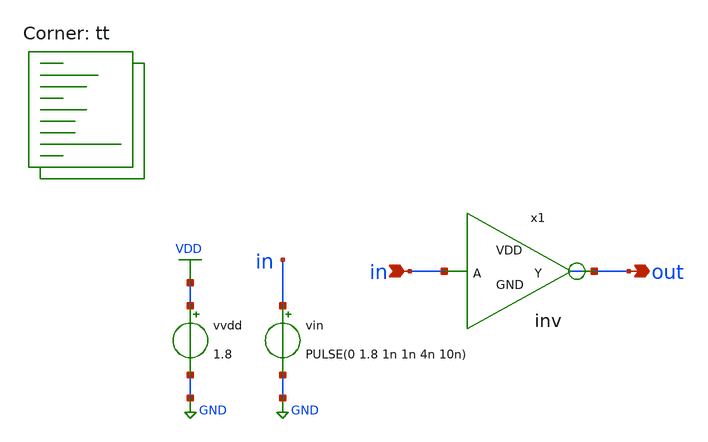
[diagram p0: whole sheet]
** sch_path: xschem/sim/tb_inv.sch
**.subckt tb_inv in out
*.ipin in
*.opin out
vvdd VDD GND 1.8
vin in GND PULSE(0 1.8 1n 1n 4n 10n)
x1 in out inv
**** begin user architecture code
.lib $::SKYWATER_MODELS/sky130.lib.spice tt


.control
* VTC analysis
DC vin 0 1.8 1m
save all
let VP = 1.8
let vo_mid = VP/2
let dvout = deriv(v(out))
meas DC VSW find v(in) when v(out)=vo_mid
meas DC VIL find v(in) WHEN dvout=-1 CROSS=1
meas DC VIH find v(in) WHEN dvout=-1 CROSS=2
meas DC VOL find v(out) WHEN dvout=-1 CROSS=2
meas DC VOH find v(out) WHEN dvout=-1 CROSS=1
echo VTC measurements
print VSW
print VIL
print VIH
print VOH
print VOL
echo
set filetype=binary
write tb_inv_vtc.raw v(out) v(in) dvout VSW VIL VIH VOH VOL

* Transient analysis
TRAN 0.01n 20n
save all
let VP=1.8
let per10 = Vp*0.1
let per50 = Vp*0.5
let per90 = Vp*0.9
meas TRAN t_rise  TRIG v(out) VAL=per10 rise=2  TARG v(out) VAL=per90 rise=2
meas TRAN t_fall  TRIG v(out) VAL=per90 fall=2  TARG v(out) VAL=per10 fall=2
meas TRAN t_delay  TRIG v(in) VAL=per50 rise=1 TARG v(out) VAL=per50 fall=1
echo TRAN measurements
print t_delay
print t_rise
print t_fall
echo
set filetype=binary
write tb_inv_tran.raw
.endc


**** end user architecture code
**.ends

* expanding   symbol:  /home/jstine/ecen4303/inv_test/xschem/inv.sym # of pins=2
** sym_path: xschem/inv.sym
** sch_path: xschem/inv.sch
.subckt inv A Y GND VDD
*.opin Y
*.ipin A
XM1 Y A VDD VDD sky130_fd_pr__pfet_01v8 L=0.15 W=0.42 nf=1 ad='int((nf+1)/2) * W/nf * 0.29' as='int((nf+2)/2) * W/nf * 0.29'
+ pd='2*int((nf+1)/2) * (W/nf + 0.29)' ps='2*int((nf+2)/2) * (W/nf + 0.29)' nrd='0.29 / W' nrs='0.29 / W'
+ sa=0 sb=0 sd=0 mult=1 m=1
XM2 Y A GND GND sky130_fd_pr__nfet_01v8 L=0.15 W=0.42 nf=1 ad='int((nf+1)/2) * W/nf * 0.29' as='int((nf+2)/2) * W/nf * 0.29'
+ pd='2*int((nf+1)/2) * (W/nf + 0.29)' ps='2*int((nf+2)/2) * (W/nf + 0.29)' nrd='0.29 / W' nrs='0.29 / W'
+ sa=0 sb=0 sd=0 mult=1 m=1
.ends

.GLOBAL GND
.GLOBAL VDD
.end
